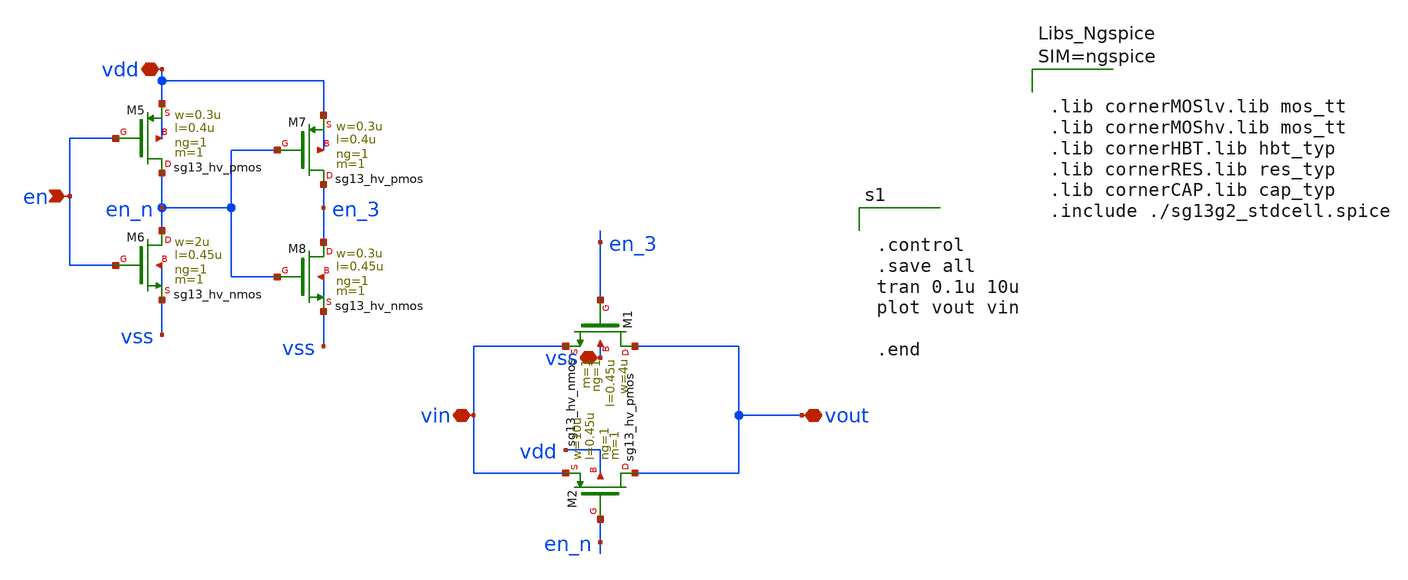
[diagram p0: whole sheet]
** sch_path: dependencies/DFT/DFT-main/schematic/xschem/schematique/switch.sch
**.subckt switch vin vout en vss vdd
*.iopin vin
*.iopin vout
*.ipin en
*.iopin vss
*.iopin vdd
XM5 en_n en vdd vdd sg13_hv_pmos w=0.3u l=0.4u ng=1 m=1 mm_ok=1
XM6 en_n en vss vss sg13_hv_nmos w=2u l=0.45u ng=1 m=1 mm_ok=1
XM7 en_3 en_n vdd vdd sg13_hv_pmos w=0.3u l=0.4u ng=1 m=1 mm_ok=1
XM8 en_3 en_n vss vss sg13_hv_nmos w=0.3u l=0.45u ng=1 m=1 mm_ok=1
XM1 vout en_3 vin vss sg13_hv_nmos w=4u l=0.45u ng=1 m=1 mm_ok=1
XM2 vout en_n vin vdd sg13_hv_pmos w=10u l=0.45u ng=1 m=1 mm_ok=1
**** begin user architecture code



.lib cornerMOSlv.lib mos_tt
.lib cornerMOShv.lib mos_tt
.lib cornerHBT.lib hbt_typ
.lib cornerRES.lib res_typ
.lib cornerCAP.lib cap_typ
.include ./sg13g2_stdcell.spice





.control
.save all
tran 0.1u 10u
plot vout vin

.end


**** end user architecture code
**.ends
.end
